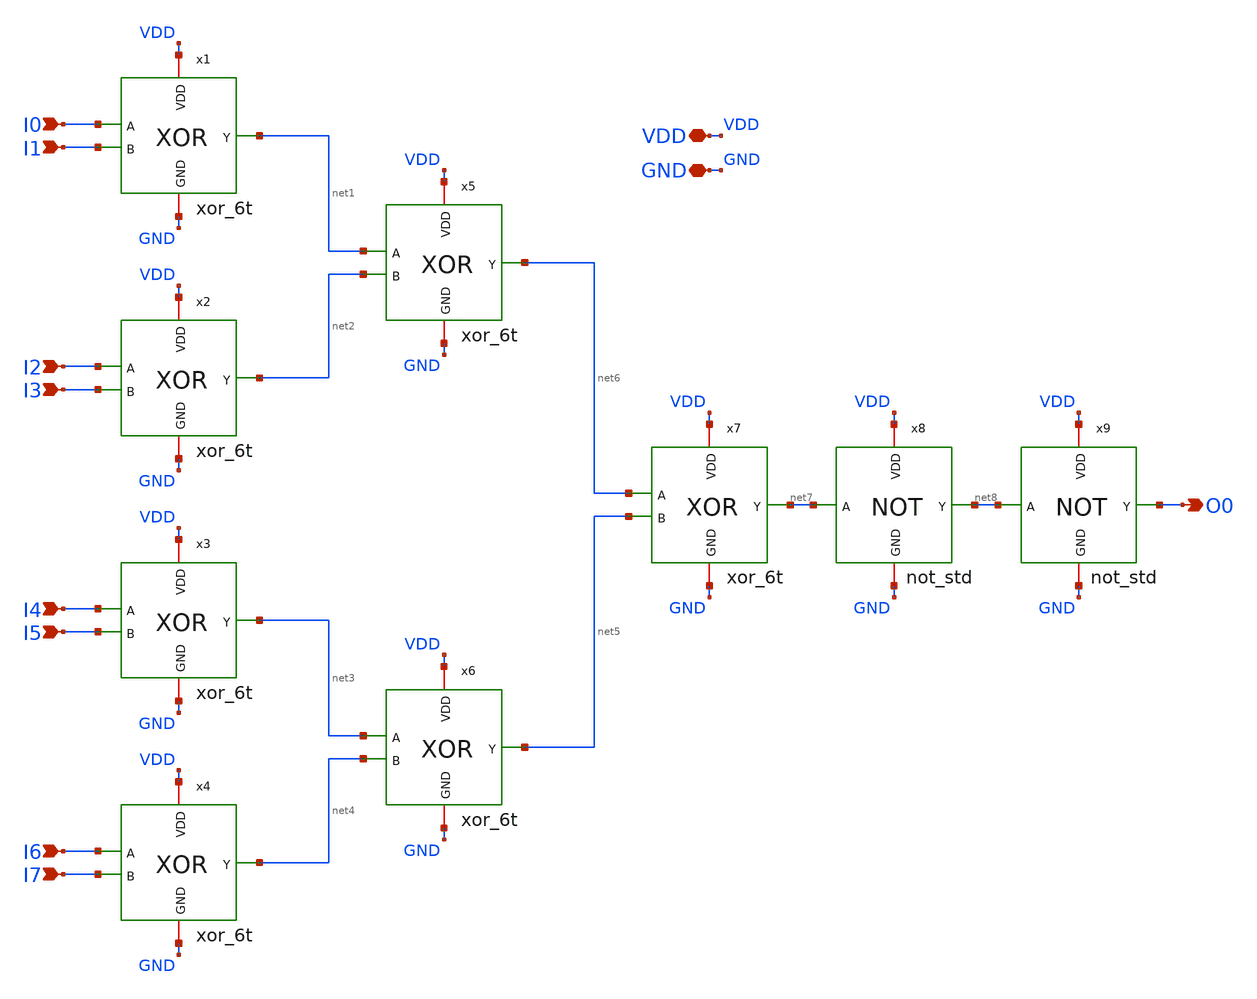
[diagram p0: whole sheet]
** sch_path: even_parity_generator/schematic/even_parity_gen_xor_6t_buf.sch
**.subckt even_parity_gen_xor_6t_buf VDD GND I0 I1 I2 I3 I4 I5 I6 I7 O0
*.iopin VDD
*.iopin GND
*.ipin I0
*.ipin I1
*.ipin I2
*.ipin I3
*.ipin I4
*.ipin I5
*.ipin I6
*.ipin I7
*.opin O0
x1 VDD net1 I0 I1 GND xor_6t
x2 VDD net2 I2 I3 GND xor_6t
x3 VDD net3 I4 I5 GND xor_6t
x4 VDD net4 I6 I7 GND xor_6t
x5 VDD net6 net1 net2 GND xor_6t
x6 VDD net5 net3 net4 GND xor_6t
x7 VDD net7 net6 net5 GND xor_6t
x8 VDD net7 net8 GND not_std
x9 VDD net8 O0 GND not_std
**.ends
.end
